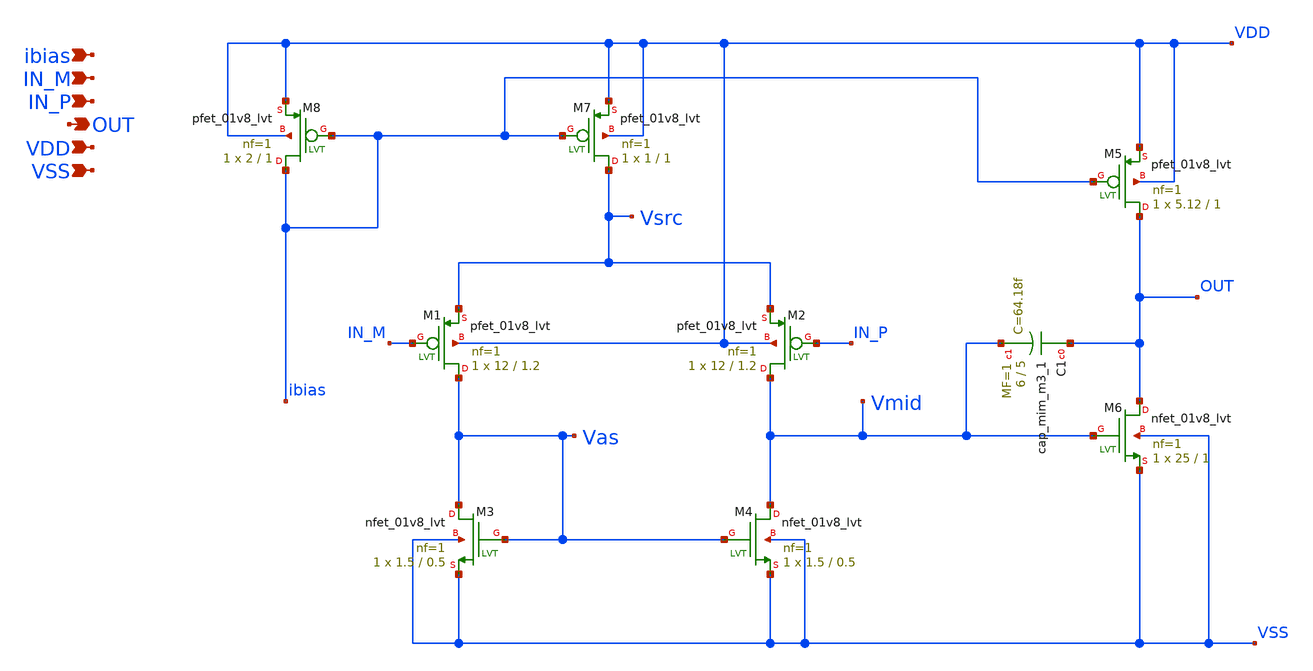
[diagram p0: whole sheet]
** sch_path: analog/xschem/OTA.sch
**.subckt OTA IN_M IN_P ibias VDD VSS OUT
*.ipin IN_M
*.ipin IN_P
*.ipin ibias
*.ipin VDD
*.ipin VSS
*.opin OUT
XM2 Vmid IN_P Vsrc VDD sky130_fd_pr__pfet_01v8_lvt L=1.2 W=12 nf=1 ad='int((nf+1)/2) * W/nf * 0.29' as='int((nf+2)/2) * W/nf * 0.29'
+ pd='2*int((nf+1)/2) * (W/nf + 0.29)' ps='2*int((nf+2)/2) * (W/nf + 0.29)' nrd='0.29 / W' nrs='0.29 / W'
+ sa=0 sb=0 sd=0 mult=1 m=1
XM1 Vas IN_M Vsrc VDD sky130_fd_pr__pfet_01v8_lvt L=1.2 W=12 nf=1 ad='int((nf+1)/2) * W/nf * 0.29' as='int((nf+2)/2) * W/nf * 0.29'
+ pd='2*int((nf+1)/2) * (W/nf + 0.29)' ps='2*int((nf+2)/2) * (W/nf + 0.29)' nrd='0.29 / W' nrs='0.29 / W'
+ sa=0 sb=0 sd=0 mult=1 m=1
XM5 OUT ibias VDD VDD sky130_fd_pr__pfet_01v8_lvt L=1 W=5.12 nf=1 ad='int((nf+1)/2) * W/nf * 0.29' as='int((nf+2)/2) * W/nf * 0.29'
+ pd='2*int((nf+1)/2) * (W/nf + 0.29)' ps='2*int((nf+2)/2) * (W/nf + 0.29)' nrd='0.29 / W' nrs='0.29 / W'
+ sa=0 sb=0 sd=0 mult=1 m=1
XM4 Vmid Vas VSS VSS sky130_fd_pr__nfet_01v8_lvt L=0.5 W=1.5 nf=1 ad='int((nf+1)/2) * W/nf * 0.29' as='int((nf+2)/2) * W/nf * 0.29'
+ pd='2*int((nf+1)/2) * (W/nf + 0.29)' ps='2*int((nf+2)/2) * (W/nf + 0.29)' nrd='0.29 / W' nrs='0.29 / W'
+ sa=0 sb=0 sd=0 mult=1 m=1
XM3 Vas Vas VSS VSS sky130_fd_pr__nfet_01v8_lvt L=0.5 W=1.5 nf=1 ad='int((nf+1)/2) * W/nf * 0.29' as='int((nf+2)/2) * W/nf * 0.29'
+ pd='2*int((nf+1)/2) * (W/nf + 0.29)' ps='2*int((nf+2)/2) * (W/nf + 0.29)' nrd='0.29 / W' nrs='0.29 / W'
+ sa=0 sb=0 sd=0 mult=1 m=1
XM6 OUT Vmid VSS VSS sky130_fd_pr__nfet_01v8_lvt L=1 W=25 nf=1 ad='int((nf+1)/2) * W/nf * 0.29' as='int((nf+2)/2) * W/nf * 0.29'
+ pd='2*int((nf+1)/2) * (W/nf + 0.29)' ps='2*int((nf+2)/2) * (W/nf + 0.29)' nrd='0.29 / W' nrs='0.29 / W'
+ sa=0 sb=0 sd=0 mult=1 m=1
XM7 Vsrc ibias VDD VDD sky130_fd_pr__pfet_01v8_lvt L=1 W=1 nf=1 ad='int((nf+1)/2) * W/nf * 0.29' as='int((nf+2)/2) * W/nf * 0.29'
+ pd='2*int((nf+1)/2) * (W/nf + 0.29)' ps='2*int((nf+2)/2) * (W/nf + 0.29)' nrd='0.29 / W' nrs='0.29 / W'
+ sa=0 sb=0 sd=0 mult=1 m=1
XM8 ibias ibias VDD VDD sky130_fd_pr__pfet_01v8_lvt L=1 W=2 nf=1 ad='int((nf+1)/2) * W/nf * 0.29' as='int((nf+2)/2) * W/nf * 0.29'
+ pd='2*int((nf+1)/2) * (W/nf + 0.29)' ps='2*int((nf+2)/2) * (W/nf + 0.29)' nrd='0.29 / W' nrs='0.29 / W'
+ sa=0 sb=0 sd=0 mult=1 m=1
XC1 OUT Vmid sky130_fd_pr__cap_mim_m3_1 W=6 L=5 MF=1 m=1
**.ends
.end
